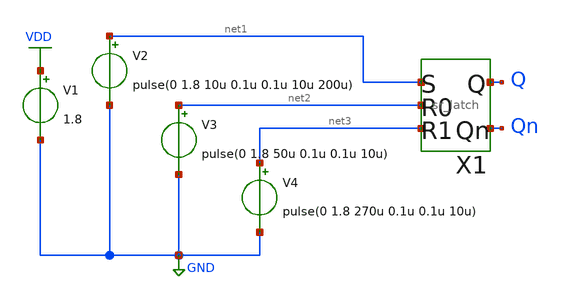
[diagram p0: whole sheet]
** sch_path: xschem/sr_latch_tb.sch
**.subckt sr_latch_tb
X1 net1 net2 Q Qn net3 sr_latch
V1 VDD GND 1.8
V2 net1 GND pulse(0 1.8 10u 0.1u 0.1u 10u 200u)
V3 net2 GND pulse(0 1.8 50u 0.1u 0.1u 10u)
V4 net3 GND pulse(0 1.8 270u 0.1u 0.1u 10u)
**** begin user architecture code


.option wnflag=1
.lib /usr/local/share/pdk/sky130A/libs.tech/ngspice/sky130.lib.spice tt
.tran 0.05u 300u
.save all


**** end user architecture code
**.ends

* expanding   symbol:  sr_latch.sym # of pins=5
** sym_path: xschem/sr_latch.sym
** sch_path: xschem/sr_latch.sch
.subckt sr_latch s r0 q qn r1
*.ipin s
*.ipin r0
*.opin qn
*.opin q
*.ipin r1
XM1 qn q net1 VDD sky130_fd_pr__pfet_01v8 L=0.15 W=1 nf=1 ad='int((1 + 1)/2) * 1 / 1 * 0.29' as='int((1 + 2)/2) * 1 / 1 * 0.29'
+ pd='2*int((1 + 1)/2) * (1 / 1 + 0.29)' ps='2*int((1 + 2)/2) * (1 / 1 + 0.29)' nrd='0.29 / 1 ' nrs='0.29 / 1 '
+ sa=0 sb=0 sd=0 mult=1 m=1
XM2 net1 s VDD VDD sky130_fd_pr__pfet_01v8 L=0.15 W=1 nf=1 ad='int((1 + 1)/2) * 1 / 1 * 0.29' as='int((1 + 2)/2) * 1 / 1 * 0.29'
+ pd='2*int((1 + 1)/2) * (1 / 1 + 0.29)' ps='2*int((1 + 2)/2) * (1 / 1 + 0.29)' nrd='0.29 / 1 ' nrs='0.29 / 1 '
+ sa=0 sb=0 sd=0 mult=1 m=1
XM3 qn s GND GND sky130_fd_pr__nfet_01v8 L=0.15 W=1 nf=1 ad='int((1 + 1)/2) * 1 / 1 * 0.29' as='int((1 + 2)/2) * 1 / 1 * 0.29'
+ pd='2*int((1 + 1)/2) * (1 / 1 + 0.29)' ps='2*int((1 + 2)/2) * (1 / 1 + 0.29)' nrd='0.29 / 1 ' nrs='0.29 / 1 '
+ sa=0 sb=0 sd=0 mult=1 m=1
XM4 qn q GND GND sky130_fd_pr__nfet_01v8 L=0.15 W=1 nf=1 ad='int((1 + 1)/2) * 1 / 1 * 0.29' as='int((1 + 2)/2) * 1 / 1 * 0.29'
+ pd='2*int((1 + 1)/2) * (1 / 1 + 0.29)' ps='2*int((1 + 2)/2) * (1 / 1 + 0.29)' nrd='0.29 / 1 ' nrs='0.29 / 1 '
+ sa=0 sb=0 sd=0 mult=1 m=1
XM5 q qn net2 VDD sky130_fd_pr__pfet_01v8 L=0.15 W=1 nf=1 ad='int((1 + 1)/2) * 1 / 1 * 0.29' as='int((1 + 2)/2) * 1 / 1 * 0.29'
+ pd='2*int((1 + 1)/2) * (1 / 1 + 0.29)' ps='2*int((1 + 2)/2) * (1 / 1 + 0.29)' nrd='0.29 / 1 ' nrs='0.29 / 1 '
+ sa=0 sb=0 sd=0 mult=1 m=1
XM6 net2 r0 net3 VDD sky130_fd_pr__pfet_01v8 L=0.15 W=1 nf=1 ad='int((1 + 1)/2) * 1 / 1 * 0.29' as='int((1 + 2)/2) * 1 / 1 * 0.29'
+ pd='2*int((1 + 1)/2) * (1 / 1 + 0.29)' ps='2*int((1 + 2)/2) * (1 / 1 + 0.29)' nrd='0.29 / 1 ' nrs='0.29 / 1 '
+ sa=0 sb=0 sd=0 mult=1 m=1
XM7 q r0 GND GND sky130_fd_pr__nfet_01v8 L=0.15 W=1 nf=1 ad='int((1 + 1)/2) * 1 / 1 * 0.29' as='int((1 + 2)/2) * 1 / 1 * 0.29'
+ pd='2*int((1 + 1)/2) * (1 / 1 + 0.29)' ps='2*int((1 + 2)/2) * (1 / 1 + 0.29)' nrd='0.29 / 1 ' nrs='0.29 / 1 '
+ sa=0 sb=0 sd=0 mult=1 m=1
XM8 q qn GND GND sky130_fd_pr__nfet_01v8 L=0.15 W=1 nf=1 ad='int((1 + 1)/2) * 1 / 1 * 0.29' as='int((1 + 2)/2) * 1 / 1 * 0.29'
+ pd='2*int((1 + 1)/2) * (1 / 1 + 0.29)' ps='2*int((1 + 2)/2) * (1 / 1 + 0.29)' nrd='0.29 / 1 ' nrs='0.29 / 1 '
+ sa=0 sb=0 sd=0 mult=1 m=1
XM9 net3 r1 VDD VDD sky130_fd_pr__pfet_01v8 L=0.15 W=1 nf=1 ad='int((1 + 1)/2) * 1 / 1 * 0.29' as='int((1 + 2)/2) * 1 / 1 * 0.29'
+ pd='2*int((1 + 1)/2) * (1 / 1 + 0.29)' ps='2*int((1 + 2)/2) * (1 / 1 + 0.29)' nrd='0.29 / 1 ' nrs='0.29 / 1 '
+ sa=0 sb=0 sd=0 mult=1 m=1
XM10 q r1 GND GND sky130_fd_pr__nfet_01v8 L=0.15 W=1 nf=1 ad='int((1 + 1)/2) * 1 / 1 * 0.29' as='int((1 + 2)/2) * 1 / 1 * 0.29'
+ pd='2*int((1 + 1)/2) * (1 / 1 + 0.29)' ps='2*int((1 + 2)/2) * (1 / 1 + 0.29)' nrd='0.29 / 1 ' nrs='0.29 / 1 '
+ sa=0 sb=0 sd=0 mult=1 m=1
.ends

.GLOBAL VDD
.GLOBAL GND
.end
